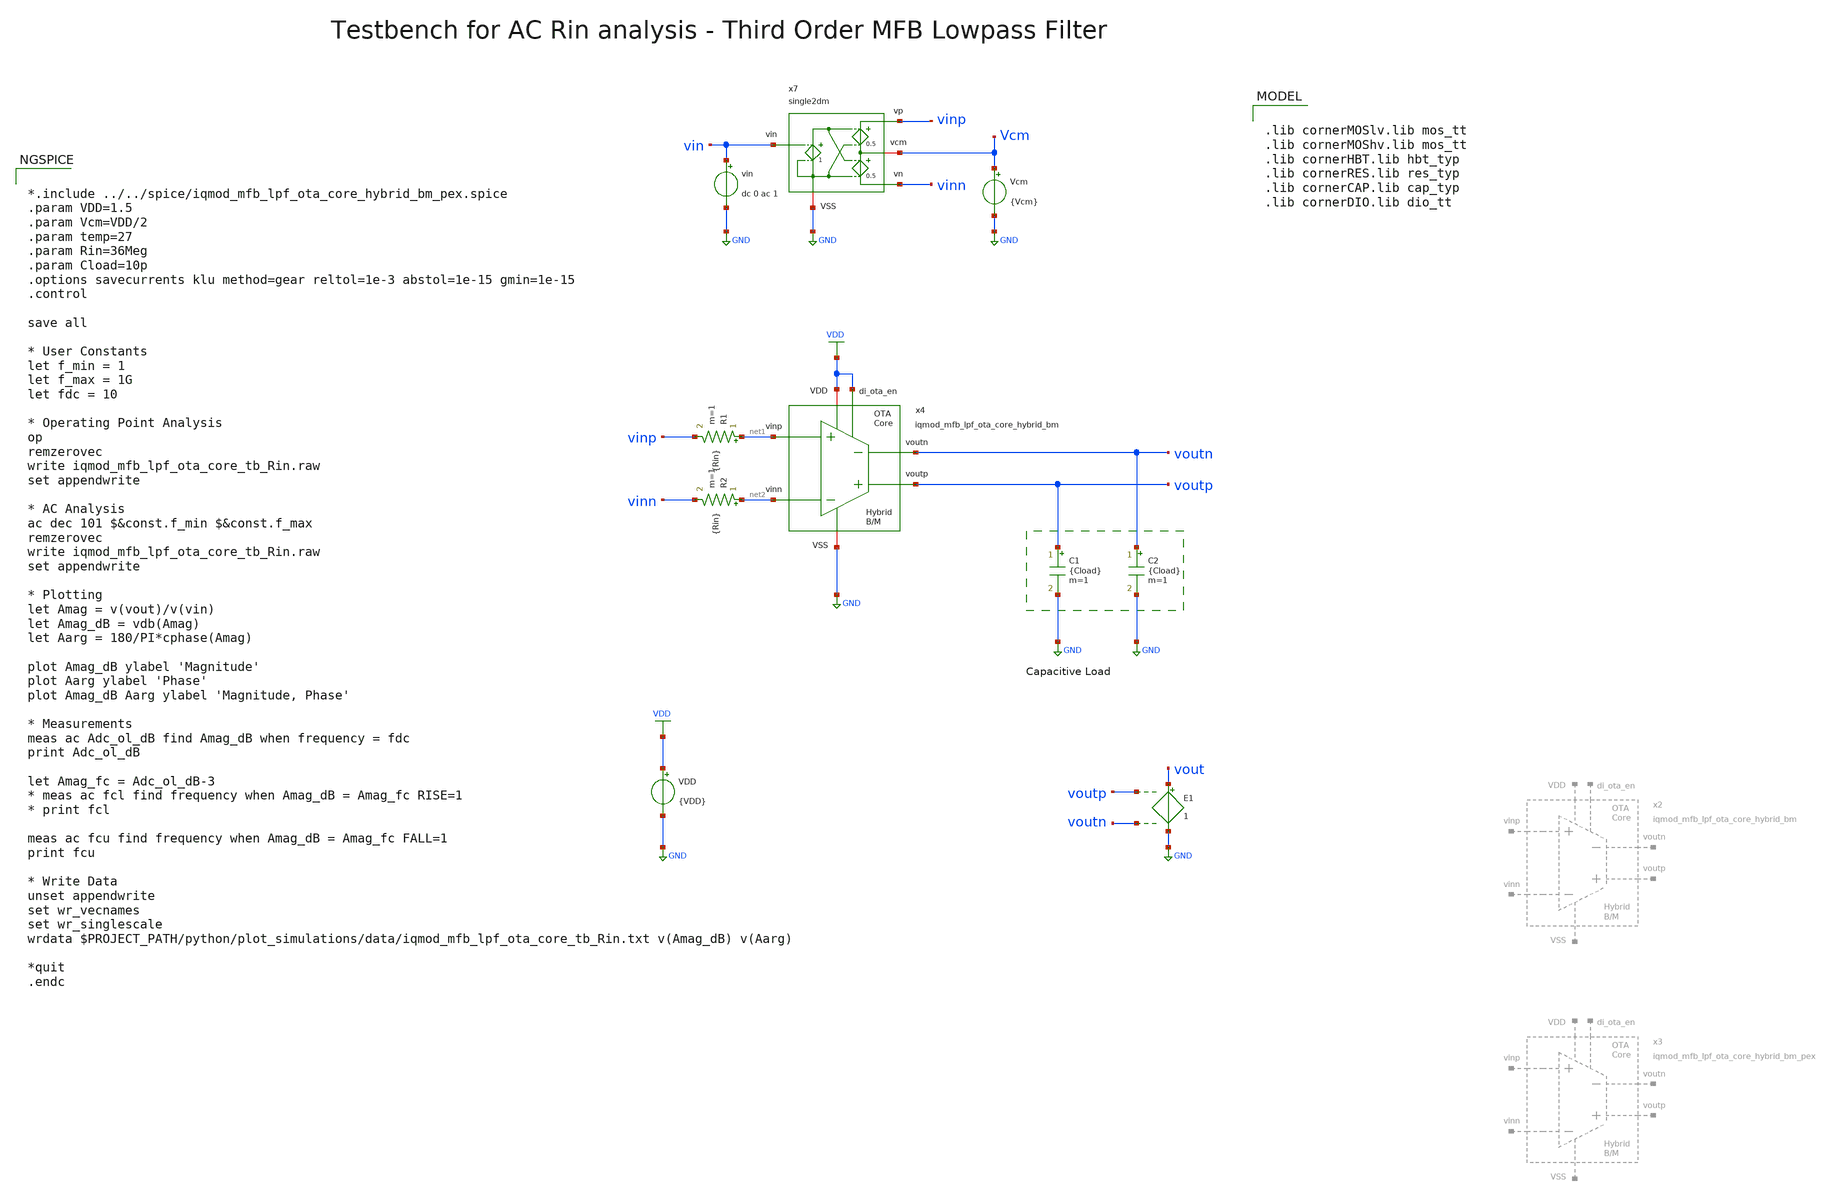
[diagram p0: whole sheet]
** sch_path: ihp130/macros/iqmod/xschem/testbenches/iqmod_mfb_lpf_ota_core_tb_Rin.sch
**.subckt iqmod_mfb_lpf_ota_core_tb_Rin
VDD VDD GND {VDD}
Vcm Vcm GND {Vcm}
E1 vout GND voutp voutn 1
vin vin GND dc 0 ac 1
R1 net1 vinp {Rin} m=1
R2 net2 vinn {Rin} m=1
C1 voutp GND {Cload} m=1
C2 voutn GND {Cload} m=1
x4 voutp voutn net2 net1 VDD GND VDD iqmod_mfb_lpf_ota_core_hybrid_bm
x7 vinp vin Vcm GND vinn single2dm
**** begin user architecture code


*.include ../../spice/iqmod_mfb_lpf_ota_core_hybrid_bm_pex.spice
.param VDD=1.5
.param Vcm=VDD/2
.param temp=27
.param Rin=36Meg
.param Cload=10p
.options savecurrents klu method=gear reltol=1e-3 abstol=1e-15 gmin=1e-15
.control

save all

* User Constants
let f_min = 1
let f_max = 1G
let fdc = 10

* Operating Point Analysis
op
remzerovec
write iqmod_mfb_lpf_ota_core_tb_Rin.raw
set appendwrite

* AC Analysis
ac dec 101 $&const.f_min $&const.f_max
remzerovec
write iqmod_mfb_lpf_ota_core_tb_Rin.raw
set appendwrite

* Plotting
let Amag = v(vout)/v(vin)
let Amag_dB = vdb(Amag)
let Aarg = 180/PI*cphase(Amag)

plot Amag_dB ylabel 'Magnitude'
plot Aarg ylabel 'Phase'
plot Amag_dB Aarg ylabel 'Magnitude, Phase'

* Measurements
meas ac Adc_ol_dB find Amag_dB when frequency = fdc
print Adc_ol_dB

let Amag_fc = Adc_ol_dB-3
* meas ac fcl find frequency when Amag_dB = Amag_fc RISE=1
* print fcl

meas ac fcu find frequency when Amag_dB = Amag_fc FALL=1
print fcu

* Write Data
unset appendwrite
set wr_vecnames
set wr_singlescale
wrdata $PROJECT_PATH/python/plot_simulations/data/iqmod_mfb_lpf_ota_core_tb_Rin.txt v(Amag_dB)
+ v(Aarg)

*quit
.endc



.lib cornerMOSlv.lib mos_tt
.lib cornerMOShv.lib mos_tt
.lib cornerHBT.lib hbt_typ
.lib cornerRES.lib res_typ
.lib cornerCAP.lib cap_typ
.lib cornerDIO.lib dio_tt

**** end user architecture code
**.ends
.GLOBAL GND
.GLOBAL VDD
.end
